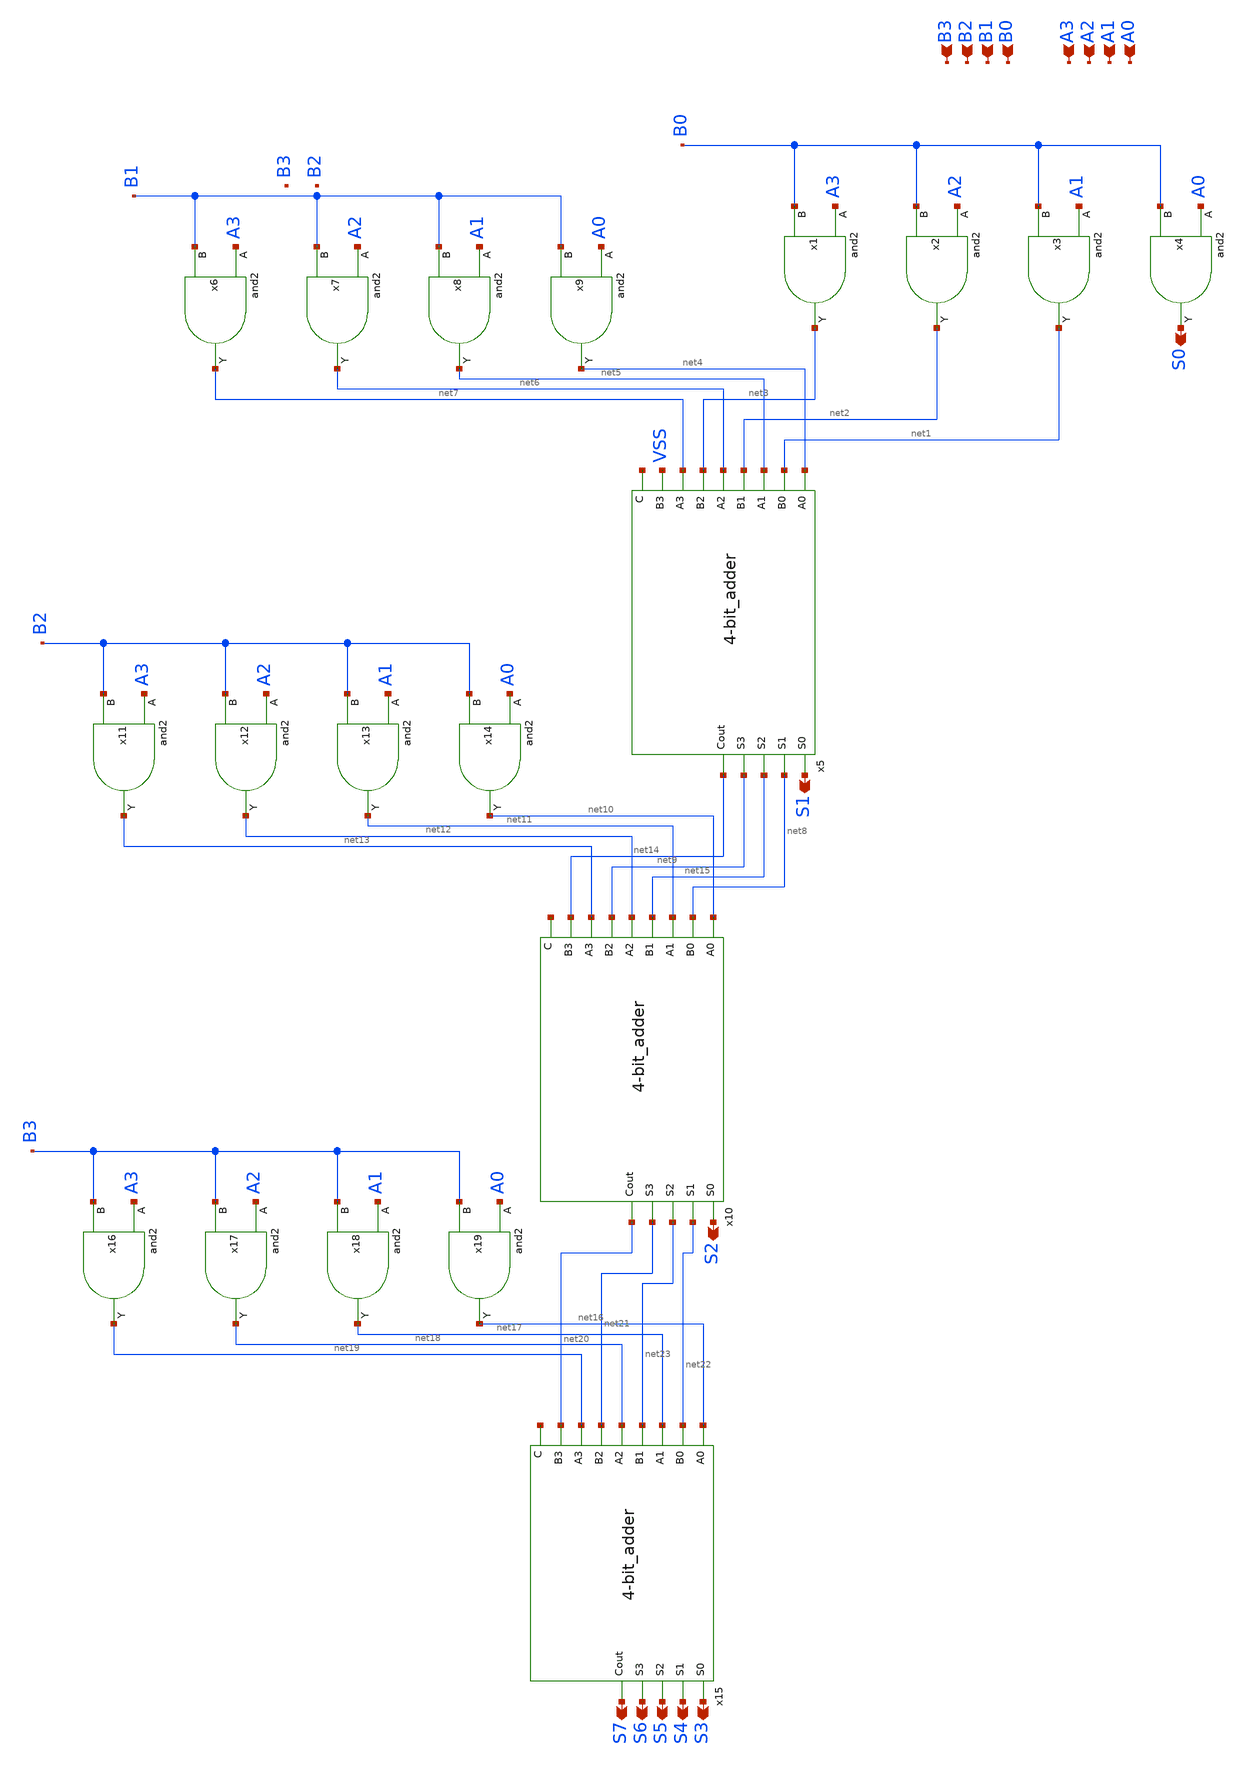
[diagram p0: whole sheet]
** sch_path: design/xschem/MULTIPLIER/mul.sch
**.subckt mul A0 A1 A2 A3 B1 B2 B3 B0 S6 S7 S3 S4 S5 S0 S1 S2
*.ipin A0
*.ipin A1
*.ipin A2
*.ipin A3
*.ipin B1
*.ipin B2
*.ipin B3
*.ipin B0
*.opin S6
*.opin S7
*.opin S3
*.opin S4
*.opin S5
*.opin S0
*.opin S1
*.opin S2
x1 A3 B0 VSS VDD net3 and2
x2 A2 B0 VSS VDD net2 and2
x3 A1 B0 VSS VDD net1 and2
x4 A0 B0 VSS VDD S0 and2
x5 net4 S1 net1 net5 net8 net2 net6 net15 net3 net7 net9 VSS net14 net24 4-bit_adder
x6 A3 B1 VSS VDD net7 and2
x7 A2 B1 VSS VDD net6 and2
x8 A1 B1 VSS VDD net5 and2
x9 A0 B1 VSS VDD net4 and2
x10 net10 S2 net8 net11 net22 net15 net12 net23 net9 net13 net21 net14 net20 net25 4-bit_adder
x11 A3 B2 VSS VDD net13 and2
x12 A2 B2 VSS VDD net12 and2
x13 A1 B2 VSS VDD net11 and2
x14 A0 B2 VSS VDD net10 and2
x15 net16 S3 net22 net17 S4 net23 net18 S5 net21 net19 S6 net20 S7 net26 4-bit_adder
x16 A3 B3 VSS VDD net19 and2
x17 A2 B3 VSS VDD net18 and2
x18 A1 B3 VSS VDD net17 and2
x19 A0 B3 VSS VDD net16 and2
**.ends

* expanding   symbol:  AND/and2.sym # of pins=3
** sym_path: design/xschem/AND/and2.sym
** sch_path: design/xschem/AND/and2.sch
.subckt and2 A B VSS VDD Y
*.ipin A
*.ipin B
*.opin Y
x1 net1 VSS VDD Y inv
x2 A B VSS VDD net1 nand2
.ends


* expanding   symbol:  ADDER/4-bit_adder.sym # of pins=14
** sym_path: design/xschem/ADDER/4-bit_adder.sym
** sch_path: design/xschem/ADDER/4-bit_adder.sch
.subckt 4-bit_adder A0 S0 B0 A1 S1 B1 A2 S2 B2 A3 S3 B3 Cout C
*.ipin C
*.opin Cout
*.opin S3
*.opin S0
*.opin S1
*.opin S2
*.ipin A0
*.ipin B0
*.ipin A1
*.ipin B1
*.ipin A2
*.ipin B2
*.ipin A3
*.ipin B3
x1 A0 S0 B0 C net1 full_adder
x2 A1 S1 B1 net1 net2 full_adder
x3 A2 S2 B2 net2 net3 full_adder
x4 A3 S3 B3 net3 Cout full_adder
.ends


* expanding   symbol:  INV/inv.sym # of pins=2
** sym_path: design/xschem/INV/inv.sym
** sch_path: design/xschem/INV/inv.sch
.subckt inv A VSS VDD Y
*.ipin A
*.opin Y
XM2 Y A VSS GND sky130_fd_pr__nfet_01v8 L=0.15 W=1 nf=1 ad='int((nf+1)/2) * W/nf * 0.29' as='int((nf+2)/2) * W/nf * 0.29'
+ pd='2*int((nf+1)/2) * (W/nf + 0.29)' ps='2*int((nf+2)/2) * (W/nf + 0.29)' nrd='0.29 / W' nrs='0.29 / W'
+ sa=0 sb=0 sd=0 mult=1 m=1
XM1 Y A VDD VDD sky130_fd_pr__pfet_01v8 L=0.15 W=3.21 nf=1 ad='int((nf+1)/2) * W/nf * 0.29' as='int((nf+2)/2) * W/nf * 0.29'
+ pd='2*int((nf+1)/2) * (W/nf + 0.29)' ps='2*int((nf+2)/2) * (W/nf + 0.29)' nrd='0.29 / W' nrs='0.29 / W'
+ sa=0 sb=0 sd=0 mult=1 m=1
.ends


* expanding   symbol:  NAND/nand2.sym # of pins=3
** sym_path: design/xschem/NAND/nand2.sym
** sch_path: design/xschem/NAND/nand2.sch
.subckt nand2 A B VSS VDD Y
*.ipin A
*.opin Y
*.ipin B
XM1 Y A VDD VDD sky130_fd_pr__pfet_01v8 L=0.15 W=3.2 nf=1 ad='int((nf+1)/2) * W/nf * 0.29' as='int((nf+2)/2) * W/nf * 0.29'
+ pd='2*int((nf+1)/2) * (W/nf + 0.29)' ps='2*int((nf+2)/2) * (W/nf + 0.29)' nrd='0.29 / W' nrs='0.29 / W'
+ sa=0 sb=0 sd=0 mult=1 m=1
XM2 Y A net1 net1 sky130_fd_pr__nfet_01v8 L=0.15 W=2 nf=1 ad='int((nf+1)/2) * W/nf * 0.29' as='int((nf+2)/2) * W/nf * 0.29'
+ pd='2*int((nf+1)/2) * (W/nf + 0.29)' ps='2*int((nf+2)/2) * (W/nf + 0.29)' nrd='0.29 / W' nrs='0.29 / W'
+ sa=0 sb=0 sd=0 mult=1 m=1
XM3 net1 B VSS VSS sky130_fd_pr__nfet_01v8 L=0.15 W=2 nf=1 ad='int((nf+1)/2) * W/nf * 0.29' as='int((nf+2)/2) * W/nf * 0.29'
+ pd='2*int((nf+1)/2) * (W/nf + 0.29)' ps='2*int((nf+2)/2) * (W/nf + 0.29)' nrd='0.29 / W' nrs='0.29 / W'
+ sa=0 sb=0 sd=0 mult=1 m=1
XM4 Y B VDD VDD sky130_fd_pr__pfet_01v8 L=0.15 W=3.2 nf=1 ad='int((nf+1)/2) * W/nf * 0.29' as='int((nf+2)/2) * W/nf * 0.29'
+ pd='2*int((nf+1)/2) * (W/nf + 0.29)' ps='2*int((nf+2)/2) * (W/nf + 0.29)' nrd='0.29 / W' nrs='0.29 / W'
+ sa=0 sb=0 sd=0 mult=1 m=1
.ends


* expanding   symbol:  ADDER/full_adder.sym # of pins=5
** sym_path: design/xschem/ADDER/full_adder.sym
** sch_path: design/xschem/ADDER/full_adder.sch
.subckt full_adder A S B Cin Cout
*.iopin A
*.iopin B
*.iopin Cin
*.iopin S
*.iopin Cout
x2 A B net1 XOR2
x1 net1 Cin S XOR2
x3 Cin net1 VSS VDD net2 nand2
x4 A B VSS VDD net3 nand2
x5 net2 net3 VSS VDD Cout nand2
.ends


* expanding   symbol:  XOR/XOR2.sym # of pins=3
** sym_path: design/xschem/XOR/XOR2.sym
** sch_path: design/xschem/XOR/XOR2.sch
.subckt XOR2 A B OUT
*.ipin A
*.ipin B
*.opin OUT
x1 A B !B !A OUT !A A !B B VSS VDD cg4
x2 A VSS VDD !A inv
x3 B VSS VDD !B inv
.ends


* expanding   symbol:  ./CG4/cg4.sym # of pins=9
** sym_path: design/xschem/CG4/cg4.sym
** sch_path: design/xschem/CG4/cg4.sch
.subckt cg4 P3 P4 P2 P1 OUT N2 N1 N4 N3 VSS VDD
*.ipin P3
*.ipin P1
*.ipin N1
*.ipin N3
*.ipin P4
*.ipin P2
*.ipin N2
*.ipin N4
*.opin OUT
XM1 OUT N1 net1 VSS sky130_fd_pr__nfet_01v8 L=0.15 W=2 nf=1 ad='int((nf+1)/2) * W/nf * 0.29' as='int((nf+2)/2) * W/nf * 0.29'
+ pd='2*int((nf+1)/2) * (W/nf + 0.29)' ps='2*int((nf+2)/2) * (W/nf + 0.29)' nrd='0.29 / W' nrs='0.29 / W'
+ sa=0 sb=0 sd=0 mult=1 m=1
XM2 OUT N2 net2 VSS sky130_fd_pr__nfet_01v8 L=0.15 W=2 nf=1 ad='int((nf+1)/2) * W/nf * 0.29' as='int((nf+2)/2) * W/nf * 0.29'
+ pd='2*int((nf+1)/2) * (W/nf + 0.29)' ps='2*int((nf+2)/2) * (W/nf + 0.29)' nrd='0.29 / W' nrs='0.29 / W'
+ sa=0 sb=0 sd=0 mult=1 m=1
XM3 net1 N3 VSS VSS sky130_fd_pr__nfet_01v8 L=0.15 W=2 nf=1 ad='int((nf+1)/2) * W/nf * 0.29' as='int((nf+2)/2) * W/nf * 0.29'
+ pd='2*int((nf+1)/2) * (W/nf + 0.29)' ps='2*int((nf+2)/2) * (W/nf + 0.29)' nrd='0.29 / W' nrs='0.29 / W'
+ sa=0 sb=0 sd=0 mult=1 m=1
XM4 net2 N4 VSS VSS sky130_fd_pr__nfet_01v8 L=0.15 W=2 nf=1 ad='int((nf+1)/2) * W/nf * 0.29' as='int((nf+2)/2) * W/nf * 0.29'
+ pd='2*int((nf+1)/2) * (W/nf + 0.29)' ps='2*int((nf+2)/2) * (W/nf + 0.29)' nrd='0.29 / W' nrs='0.29 / W'
+ sa=0 sb=0 sd=0 mult=1 m=1
XM5 OUT P1 net3 VDD sky130_fd_pr__pfet_01v8 L=0.15 W=8.25 nf=1 ad='int((nf+1)/2) * W/nf * 0.29' as='int((nf+2)/2) * W/nf * 0.29'
+ pd='2*int((nf+1)/2) * (W/nf + 0.29)' ps='2*int((nf+2)/2) * (W/nf + 0.29)' nrd='0.29 / W' nrs='0.29 / W'
+ sa=0 sb=0 sd=0 mult=1 m=1
XM6 OUT P2 net3 VDD sky130_fd_pr__pfet_01v8 L=0.15 W=8.25 nf=1 ad='int((nf+1)/2) * W/nf * 0.29' as='int((nf+2)/2) * W/nf * 0.29'
+ pd='2*int((nf+1)/2) * (W/nf + 0.29)' ps='2*int((nf+2)/2) * (W/nf + 0.29)' nrd='0.29 / W' nrs='0.29 / W'
+ sa=0 sb=0 sd=0 mult=1 m=1
XM7 net3 P3 VDD VDD sky130_fd_pr__pfet_01v8 L=0.15 W=8.25 nf=1 ad='int((nf+1)/2) * W/nf * 0.29' as='int((nf+2)/2) * W/nf * 0.29'
+ pd='2*int((nf+1)/2) * (W/nf + 0.29)' ps='2*int((nf+2)/2) * (W/nf + 0.29)' nrd='0.29 / W' nrs='0.29 / W'
+ sa=0 sb=0 sd=0 mult=1 m=1
XM8 net3 P4 VDD VDD sky130_fd_pr__pfet_01v8 L=0.15 W=8.25 nf=1 ad='int((nf+1)/2) * W/nf * 0.29' as='int((nf+2)/2) * W/nf * 0.29'
+ pd='2*int((nf+1)/2) * (W/nf + 0.29)' ps='2*int((nf+2)/2) * (W/nf + 0.29)' nrd='0.29 / W' nrs='0.29 / W'
+ sa=0 sb=0 sd=0 mult=1 m=1
.ends

.end
